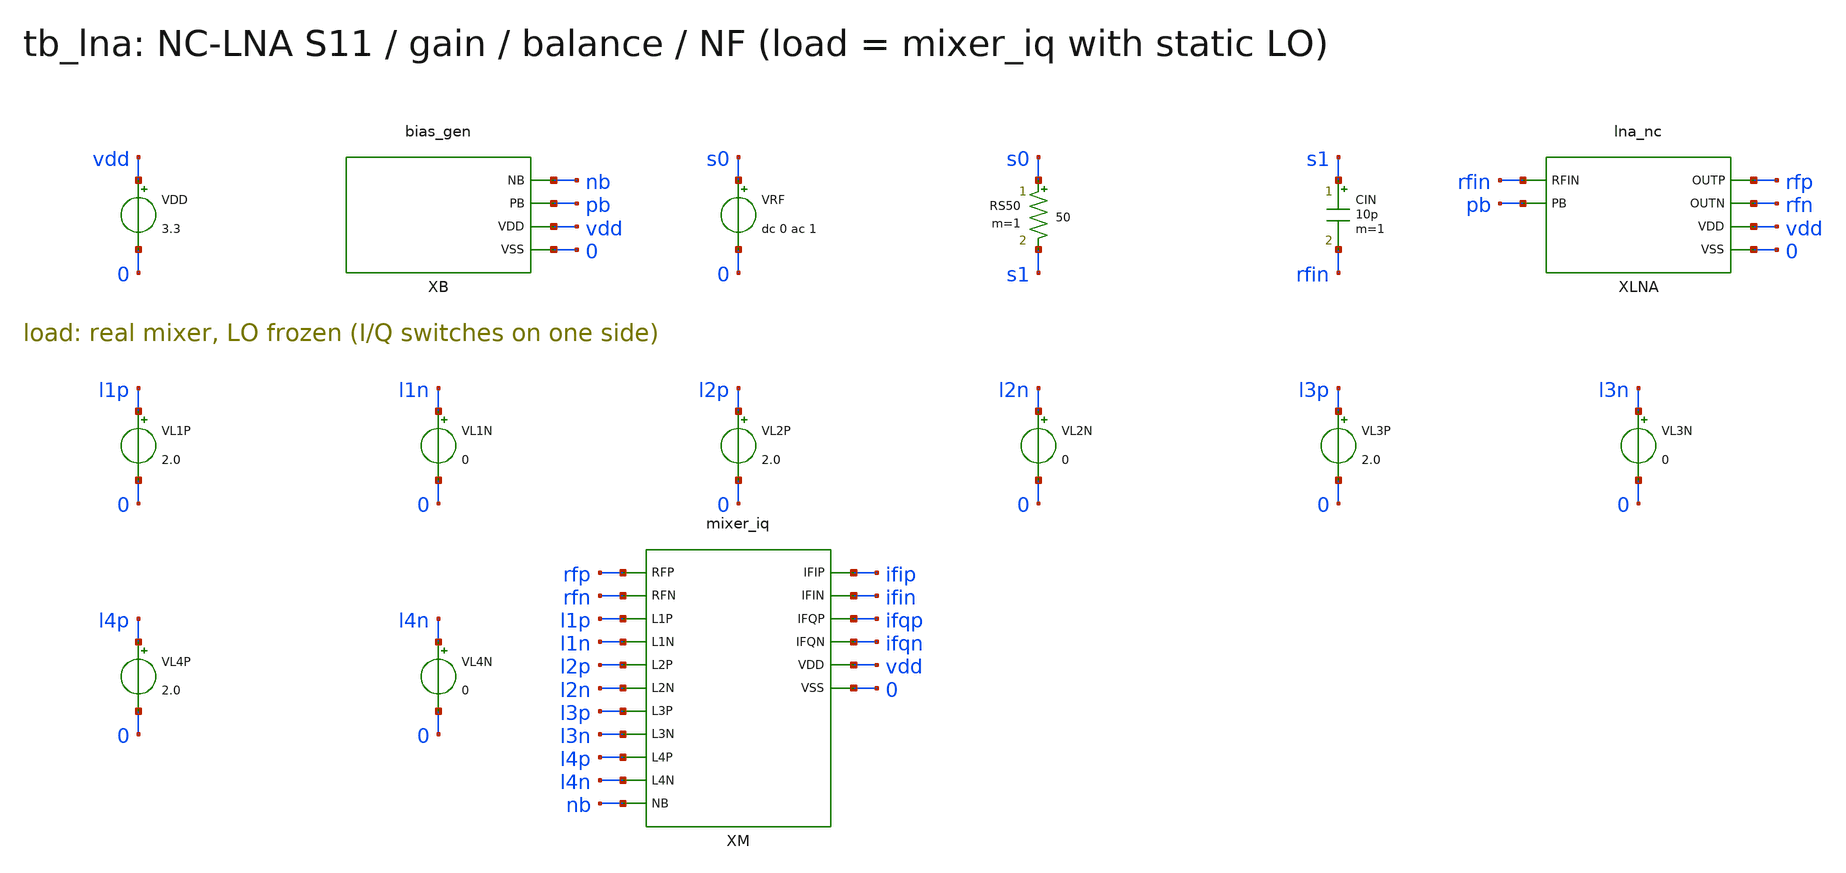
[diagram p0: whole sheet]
** sch_path: v1_claude/xschem/tb_lna.sch
**.subckt tb_lna
VDD vdd 0 3.3
XB nb pb vdd 0 bias_gen
VRF s0 0 dc 0 ac 1
RS50 s0 s1 50 m=1
CIN s1 rfin 10p m=1
XLNA rfin pb rfp rfn vdd 0 lna_nc
VL1P l1p 0 2.0
VL1N l1n 0 0
VL2P l2p 0 2.0
VL2N l2n 0 0
VL3P l3p 0 2.0
VL3N l3n 0 0
VL4P l4p 0 2.0
VL4N l4n 0 0
XM rfp rfn l1p l1n l2p l2n l3p l3n l4p l4n nb ifip ifin ifqp ifqn vdd 0 mixer_iq
**** begin user architecture code
 .include $::180MCU_MODELS/design.ngspice
.lib $::180MCU_MODELS/sm141064.ngspice typical
.lib $::180MCU_MODELS/sm141064.ngspice res_typical
.lib $::180MCU_MODELS/sm141064.ngspice mimcap_typical

.control
set num_threads=1
op
echo RES op i1=$&@m.xlna.xm1.m0[id] gm1=$&@m.xlna.xm1.m0[gm] gmb1=$&@m.xlna.xm1.m0[gmbs]
+ i2=$&@m.xlna.xm2.m0[id] gm2=$&@m.xlna.xm2.m0[gm] vx=$&v(rfin) vop=$&v(xlna.op_i) von=$&v(xlna.on_i) vb1=$&v(xlna.vb1)
+ vb2=$&v(xlna.vb2) idd=$&i(VDD)
ac lin 9 1.4e9 1.8e9
let zin = v(rfin)/(-i(VRF))
let s11 = db((zin-50)/(zin+50))
let gp = v(rfp)/v(s0)*2
let gn = v(rfn)/v(s0)*2
let gd = db((v(rfp)-v(rfn))/v(s0)*2)
let bal = db(mag(gp)/mag(gn))
let ph = (cph(gp)-cph(gn))*180/pi
print frequency real(zin) imag(zin) s11 gd bal ph
noise v(rfp,rfn) VRF lin 9 1.4e9 1.8e9
setplot noise1
let nf = 10*log10(inoise_spectrum^2/(4*1.380649e-23*300*50))
print frequency nf
.endc

**** end user architecture code
**.ends
.end
